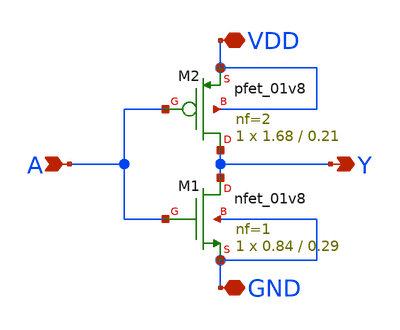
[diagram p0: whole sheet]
** sch_path: cells/INV1X4/schematic/inv1x4.sch
**.subckt inv1x4 A Y VDD GND
*.ipin A
*.opin Y
*.iopin VDD
*.iopin GND
XM1 Y A GND GND sky130_fd_pr__nfet_01v8 L=0.29 W=0.84 nf=1 ad='int((1 + 1)/2) * 0.84 / 1 * 0.29' as='int((1 + 2)/2) * 0.84 / 1 * 0.29'
+ pd='2*int((1 + 1)/2) * (0.84 / 1 + 0.29)' ps='2*int((1 + 2)/2) * (0.84 / 1 + 0.29)' nrd='0.29 / 0.84 '
+ nrs='0.29 / 0.84 ' sa=0 sb=0 sd=0 mult=1 m=1
XM2 Y A VDD VDD sky130_fd_pr__pfet_01v8 L=0.21 W=1.68 nf=2 ad='int((2 + 1)/2) * 1.68 / 2 * 0.29' as='int((2 + 2)/2) * 1.68 / 2 * 0.29'
+ pd='2*int((2 + 1)/2) * (1.68 / 2 + 0.29)' ps='2*int((2 + 2)/2) * (1.68 / 2 + 0.29)' nrd='0.29 / 1.68 '
+ nrs='0.29 / 1.68 ' sa=0 sb=0 sd=0 mult=1 m=1
**.ends
.end
